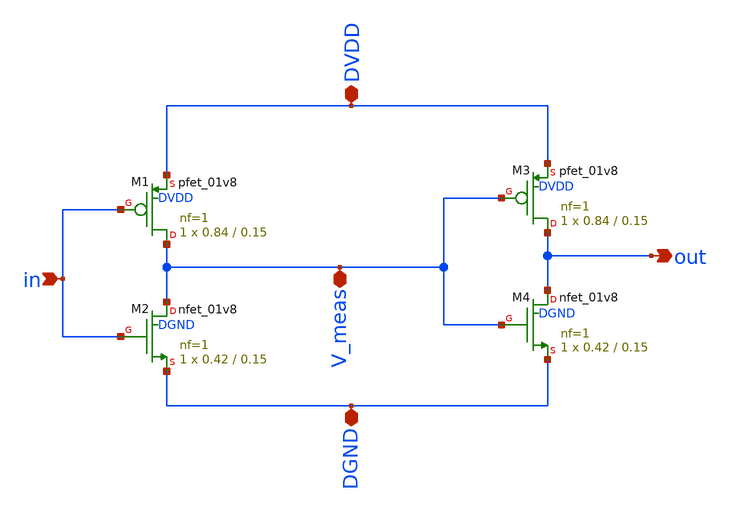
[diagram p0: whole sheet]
** sch_path: tutorial-4/source/q1b/inv2.sch
**.subckt inv2 in DVDD DGND out V_meas
*.ipin in
*.iopin DVDD
*.iopin DGND
*.opin out
*.iopin V_meas
XM1 V_meas in DVDD DVDD sky130_fd_pr__pfet_01v8 L=0.15 W=0.84 nf=1 ad='int((nf+1)/2) * W/nf * 0.29' as='int((nf+2)/2) * W/nf * 0.29'
+ pd='2*int((nf+1)/2) * (W/nf + 0.29)' ps='2*int((nf+2)/2) * (W/nf + 0.29)' nrd='0.29 / W' nrs='0.29 / W'
+ sa=0 sb=0 sd=0 mult=1 m=1
XM2 V_meas in DGND DGND sky130_fd_pr__nfet_01v8 L=0.15 W=0.42 nf=1 ad='int((nf+1)/2) * W/nf * 0.29' as='int((nf+2)/2) * W/nf * 0.29'
+ pd='2*int((nf+1)/2) * (W/nf + 0.29)' ps='2*int((nf+2)/2) * (W/nf + 0.29)' nrd='0.29 / W' nrs='0.29 / W'
+ sa=0 sb=0 sd=0 mult=1 m=1
XM3 out V_meas DVDD DVDD sky130_fd_pr__pfet_01v8 L=0.15 W=0.84 nf=1 ad='int((nf+1)/2) * W/nf * 0.29'
+ as='int((nf+2)/2) * W/nf * 0.29' pd='2*int((nf+1)/2) * (W/nf + 0.29)' ps='2*int((nf+2)/2) * (W/nf + 0.29)'
+ nrd='0.29 / W' nrs='0.29 / W' sa=0 sb=0 sd=0 mult=1 m=1
XM4 out V_meas DGND DGND sky130_fd_pr__nfet_01v8 L=0.15 W=0.42 nf=1 ad='int((nf+1)/2) * W/nf * 0.29'
+ as='int((nf+2)/2) * W/nf * 0.29' pd='2*int((nf+1)/2) * (W/nf + 0.29)' ps='2*int((nf+2)/2) * (W/nf + 0.29)'
+ nrd='0.29 / W' nrs='0.29 / W' sa=0 sb=0 sd=0 mult=1 m=1
**.ends
.end
